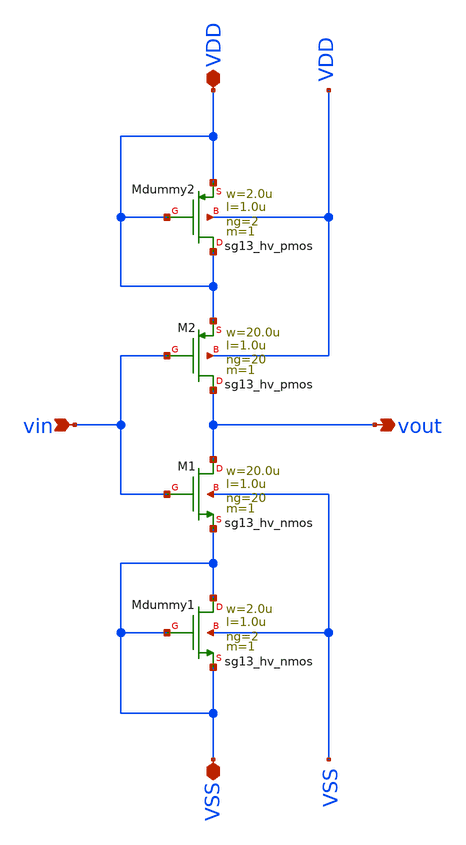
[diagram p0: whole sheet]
** sch_path: macros/heichips26_vcr/macros/switched_capacitor/schematic/xschem/low_th_inverter.sch
**.subckt low_th_inverter vin VDD VSS vout
*.ipin vin
*.iopin VDD
*.iopin VSS
*.opin vout
XMdummy1 VSS VSS VSS VSS sg13_hv_nmos w=2.0u l=1.0u ng=2 m=1 mm_ok=1
XMdummy2 VDD VDD VDD VDD sg13_hv_pmos w=2.0u l=1.0u ng=2 m=1 mm_ok=1
XM1 vout vin VSS VSS sg13_hv_nmos w=20.0u l=1.0u ng=20 m=1 mm_ok=1
XM2 vout vin VDD VDD sg13_hv_pmos w=20.0u l=1.0u ng=20 m=1 mm_ok=1
**.ends
.end
